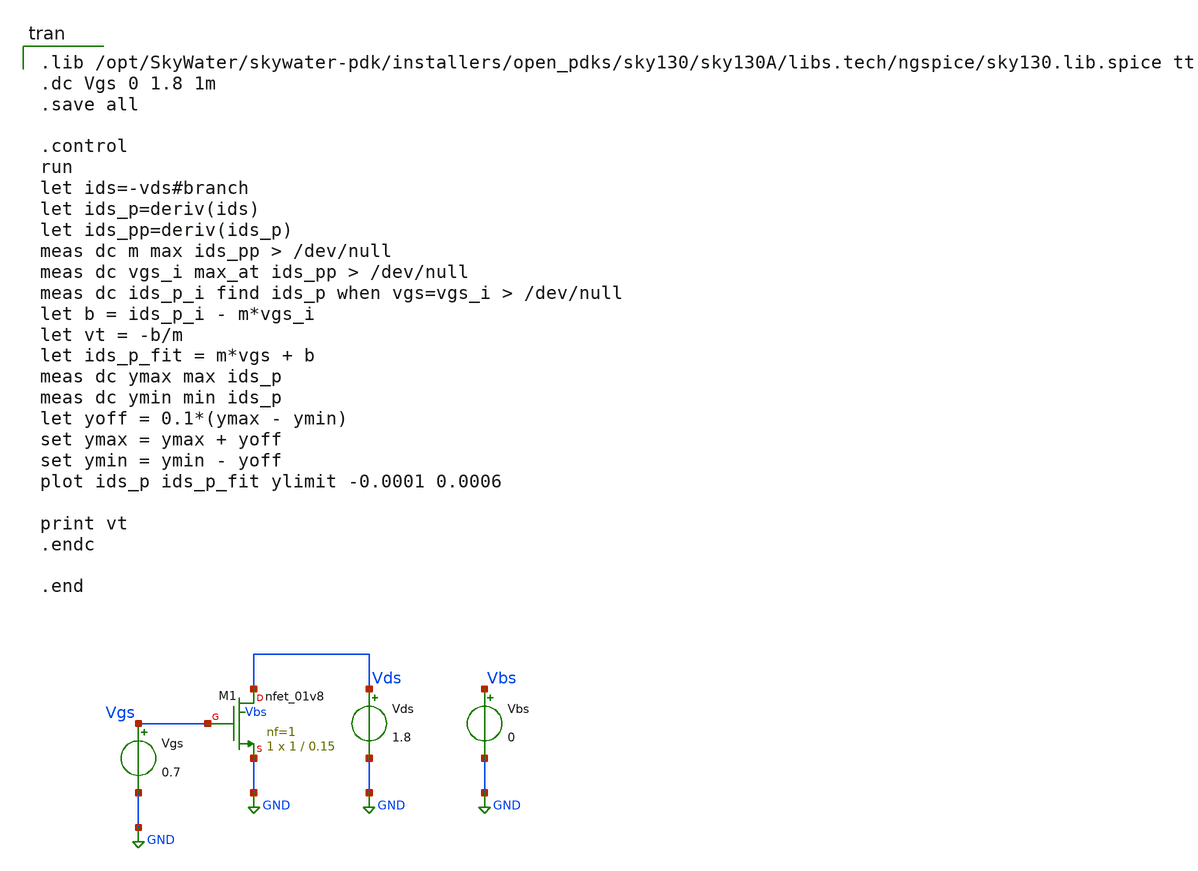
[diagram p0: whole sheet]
** sch_path: 1/xschem/nmos_iv_characteristics.sch
**.subckt nmos_iv_characteristics
XM1 Vds Vgs GND Vbs sky130_fd_pr__nfet_01v8 L=0.15 W=1 nf=1 ad='int((1 + 1)/2) * 1 / 1 * 0.29' as='int((1 + 2)/2) * 1 / 1 * 0.29'
+ pd='2*int((1 + 1)/2) * (1 / 1 + 0.29)' ps='2*int((1 + 2)/2) * (1 / 1 + 0.29)' nrd='0.29 / 1 ' nrs='0.29 / 1 '
+ sa=0 sb=0 sd=0 mult=1 m=1
Vds Vds GND 1.8
.save i(vds)
Vgs Vgs GND 0.7
.save i(vgs)
Vbs Vbs GND 0
.save i(vbs)
**** begin user architecture code

.lib /opt/SkyWater/skywater-pdk/installers/open_pdks/sky130/sky130A/libs.tech/ngspice/sky130.lib.spice tt
.dc Vgs 0 1.8 1m
.save all

.control
run
let ids=-vds#branch
let ids_p=deriv(ids)
let ids_pp=deriv(ids_p)
meas dc m max ids_pp > /dev/null
meas dc vgs_i max_at ids_pp > /dev/null
meas dc ids_p_i find ids_p when vgs=vgs_i > /dev/null
let b = ids_p_i - m*vgs_i
let vt = -b/m
let ids_p_fit = m*vgs + b
meas dc ymax max ids_p
meas dc ymin min ids_p
let yoff = 0.1*(ymax - ymin)
set ymax = ymax + yoff
set ymin = ymin - yoff
plot ids_p ids_p_fit ylimit -0.0001 0.0006

print vt
.endc

.end

**** end user architecture code
**.ends
.GLOBAL GND
.end
